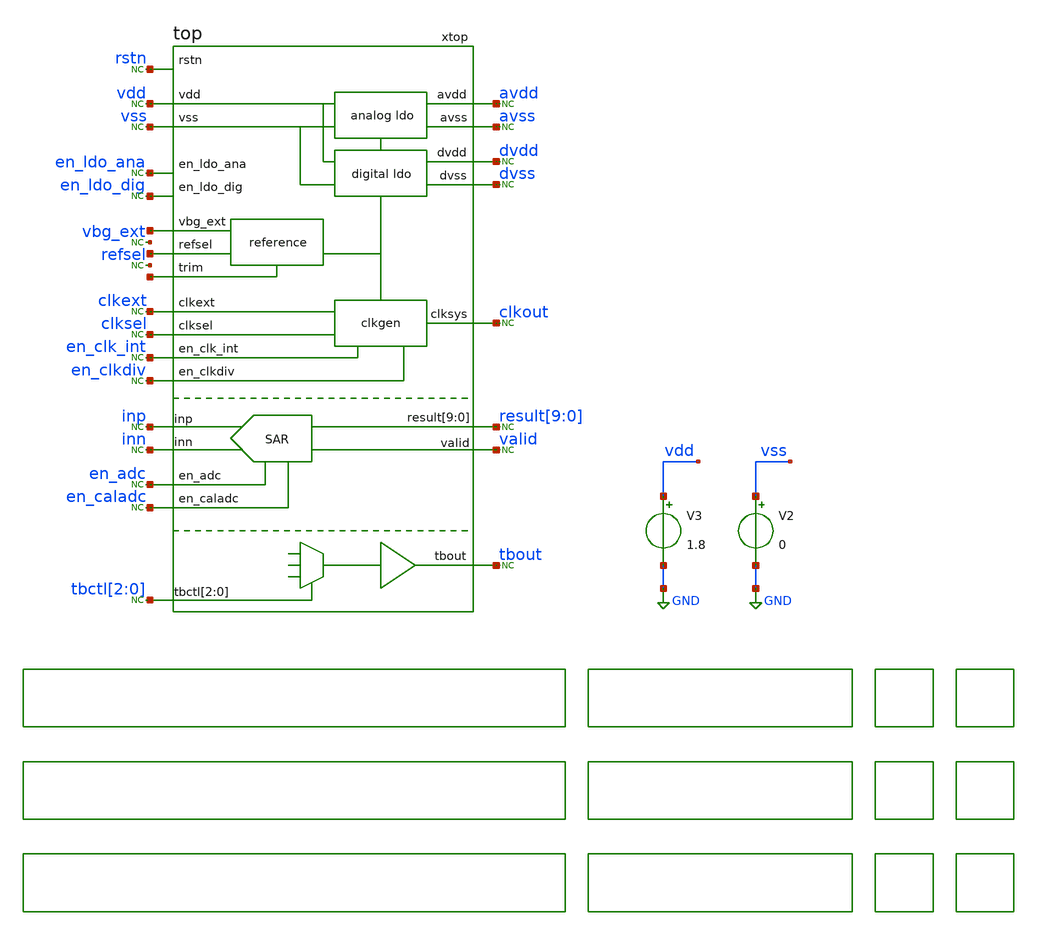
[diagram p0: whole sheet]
** sch_path: xschem/top/xschem_top.sch
**.subckt xschem_top
V2 vss GND 0
V3 vdd GND 1.8
* noconn vdd
* noconn vss
* noconn rstn
* noconn clkext
* noconn vbg_ext
* noconn en_ldo_ana
* noconn en_ldo_dig
* noconn en_clk_int
* noconn en_clkdiv
* noconn en_adc
* noconn en_caladc
* noconn clksel
* noconn refsel
* noconn inp
* noconn inn
* noconn tbout
* noconn valid
* noconn result[9:0]
xtop en_caladc dvdd inp result[9] result[8] result[7] result[6] result[5] result[4] result[3]
+ result[2] result[1] result[0] valid en_ldo_dig inn en_adc avdd rstn vdd vss en_ldo_ana clkout en_clk_int
+ clkext tbout en_clkdiv clksel net1 net2 tbctl[2] tbctl[1] tbctl[0] avss dvss net3[15] net3[14] net3[13]
+ net3[12] net3[11] net3[10] net3[9] net3[8] net3[7] net3[6] net3[5] net3[4] net3[3] net3[2] net3[1] net3[0]
+ top
* noconn tbctl[2:0]
* noconn clkout
* noconn avdd
* noconn avss
* noconn dvdd
* noconn dvss
**** begin user architecture code

.param MC_SWITCH=0

.control
save all
op
.endc


 * FET CORNERS
.include $::SKYWATER_MODELS/corners/tt.spice
*.include $::SKYWATER_MODELS/corners/ff.spice
*.include $::SKYWATER_MODELS/corners/ss.spice
*.include $::SKYWATER_MODELS/corners/sf.spice
*.include $::SKYWATER_MODELS/corners/fs.spice

* TT + R + C
*.include $::SKYWATER_MODELS/corners/tt_rmax_cmax.spice
*.include $::SKYWATER_MODELS/corners/tt_rmin_cmin.spice
*.include $::SKYWATER_MODELS/corners/tt_rmax_cmin.spice
*.include $::SKYWATER_MODELS/corners/tt_rmin_cmax.spice

* FF + R + C
*.include $::SKYWATER_MODELS/corners/ff_rmax_cmax.spice
*.include $::SKYWATER_MODELS/corners/ff_rmin_cmin.spice
*.include $::SKYWATER_MODELS/corners/ff_rmax_cmin.spice
*.include $::SKYWATER_MODELS/corners/ff_rmin_cmax.spice


* SS + R + C
*.include $::SKYWATER_MODELS/corners/ss_rmax_cmax.spice
*.include $::SKYWATER_MODELS/corners/ss_rmin_cmin.spice
*.include $::SKYWATER_MODELS/corners/ss_rmax_cmin.spice
*.include $::SKYWATER_MODELS/corners/ss_rmin_cmax.spice

* SF + R + C
*.include $::SKYWATER_MODELS/corners/sf_rmax_cmax.spice
*.include $::SKYWATER_MODELS/corners/sf_rmin_cmin.spice
*.include $::SKYWATER_MODELS/corners/sf_rmax_cmin.spice
*.include $::SKYWATER_MODELS/corners/sf_rmin_cmax.spice

* FS + R + C
*.include $::SKYWATER_MODELS/corners/fs_rmax_cmax.spice
*.include $::SKYWATER_MODELS/corners/fs_rmin_cmin.spice
*.include $::SKYWATER_MODELS/corners/fs_rmax_cmin.spice
*.include $::SKYWATER_MODELS/corners/fs_rmin_cmax.spice

[sky130_models]
**** end user architecture code
**.ends
.GLOBAL GND
.end
